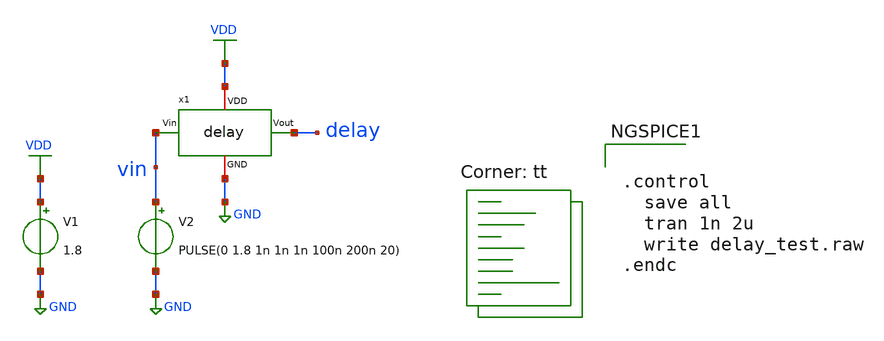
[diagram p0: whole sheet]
** sch_path: delay/delay_test.sch
**.subckt delay_test
V1 VDD GND 1.8
x1 VDD vin delay GND delay
V2 vin GND PULSE(0 1.8 1n 1n 1n 100n 200n 20)
**** begin user architecture code
.lib $::SKYWATER_MODELS/sky130.lib.spice tt

** opencircuitdesign pdks install
.inc $::SKYWATER_MODELS/rram_v0.spice



.control
  save all
  tran 1n 2u
  write delay_test.raw
.endc


**** end user architecture code
**.ends

* expanding   symbol:  /home/ricardo/RATT_repos/Proyectos_xschem/delay/delay.sym # of pins=4
** sym_path: delay/delay.sym
** sch_path: delay/delay.sch
.subckt delay VDD Vin Vout GND
*.ipin Vin
*.opin Vout
*.iopin VDD
*.iopin GND
XM1 net1 Vin VDD VDD sky130_fd_pr__pfet_01v8 L=6 W=0.45 nf=1 ad='int((nf+1)/2) * W/nf * 0.29' as='int((nf+2)/2) * W/nf * 0.29'
+ pd='2*int((nf+1)/2) * (W/nf + 0.29)' ps='2*int((nf+2)/2) * (W/nf + 0.29)' nrd='0.29 / W' nrs='0.29 / W'
+ sa=0 sb=0 sd=0 mult=1 m=1
XM2 net1 Vin GND GND sky130_fd_pr__nfet_01v8 L=6 W=0.45 nf=1 ad='int((nf+1)/2) * W/nf * 0.29' as='int((nf+2)/2) * W/nf * 0.29'
+ pd='2*int((nf+1)/2) * (W/nf + 0.29)' ps='2*int((nf+2)/2) * (W/nf + 0.29)' nrd='0.29 / W' nrs='0.29 / W'
+ sa=0 sb=0 sd=0 mult=1 m=1
XM3 net2 net1 VDD VDD sky130_fd_pr__pfet_01v8 L=6 W=0.45 nf=1 ad='int((nf+1)/2) * W/nf * 0.29' as='int((nf+2)/2) * W/nf * 0.29'
+ pd='2*int((nf+1)/2) * (W/nf + 0.29)' ps='2*int((nf+2)/2) * (W/nf + 0.29)' nrd='0.29 / W' nrs='0.29 / W'
+ sa=0 sb=0 sd=0 mult=1 m=1
XM4 net2 net1 GND GND sky130_fd_pr__nfet_01v8 L=6 W=0.45 nf=1 ad='int((nf+1)/2) * W/nf * 0.29' as='int((nf+2)/2) * W/nf * 0.29'
+ pd='2*int((nf+1)/2) * (W/nf + 0.29)' ps='2*int((nf+2)/2) * (W/nf + 0.29)' nrd='0.29 / W' nrs='0.29 / W'
+ sa=0 sb=0 sd=0 mult=1 m=1
XM5 net3 net2 VDD VDD sky130_fd_pr__pfet_01v8 L=6 W=0.45 nf=1 ad='int((nf+1)/2) * W/nf * 0.29' as='int((nf+2)/2) * W/nf * 0.29'
+ pd='2*int((nf+1)/2) * (W/nf + 0.29)' ps='2*int((nf+2)/2) * (W/nf + 0.29)' nrd='0.29 / W' nrs='0.29 / W'
+ sa=0 sb=0 sd=0 mult=1 m=1
XM6 net3 net2 GND GND sky130_fd_pr__nfet_01v8 L=6 W=0.45 nf=1 ad='int((nf+1)/2) * W/nf * 0.29' as='int((nf+2)/2) * W/nf * 0.29'
+ pd='2*int((nf+1)/2) * (W/nf + 0.29)' ps='2*int((nf+2)/2) * (W/nf + 0.29)' nrd='0.29 / W' nrs='0.29 / W'
+ sa=0 sb=0 sd=0 mult=1 m=1
XM7 Vout net3 VDD VDD sky130_fd_pr__pfet_01v8 L=6 W=0.45 nf=1 ad='int((nf+1)/2) * W/nf * 0.29' as='int((nf+2)/2) * W/nf * 0.29'
+ pd='2*int((nf+1)/2) * (W/nf + 0.29)' ps='2*int((nf+2)/2) * (W/nf + 0.29)' nrd='0.29 / W' nrs='0.29 / W'
+ sa=0 sb=0 sd=0 mult=1 m=1
XM8 Vout net3 GND GND sky130_fd_pr__nfet_01v8 L=6 W=0.45 nf=1 ad='int((nf+1)/2) * W/nf * 0.29' as='int((nf+2)/2) * W/nf * 0.29'
+ pd='2*int((nf+1)/2) * (W/nf + 0.29)' ps='2*int((nf+2)/2) * (W/nf + 0.29)' nrd='0.29 / W' nrs='0.29 / W'
+ sa=0 sb=0 sd=0 mult=1 m=1
.ends

.GLOBAL GND
.GLOBAL VDD
.end
